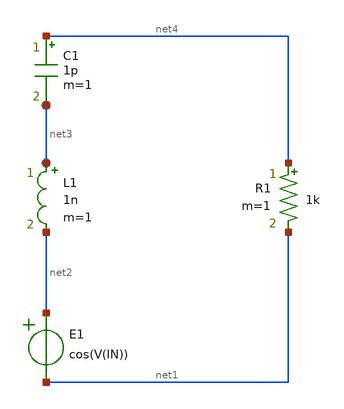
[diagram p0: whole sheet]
** sch_path: lib/Organize_into_Examples_or_pdk_examples/Example.sch
**.subckt Example
C1 net4 net3 1p m=1
R1 net4 net1 1k m=1
L1 net3 net2 1n m=1
E1 net2 net1 VOL=' cos(V(IN)) '
**.ends
.end
